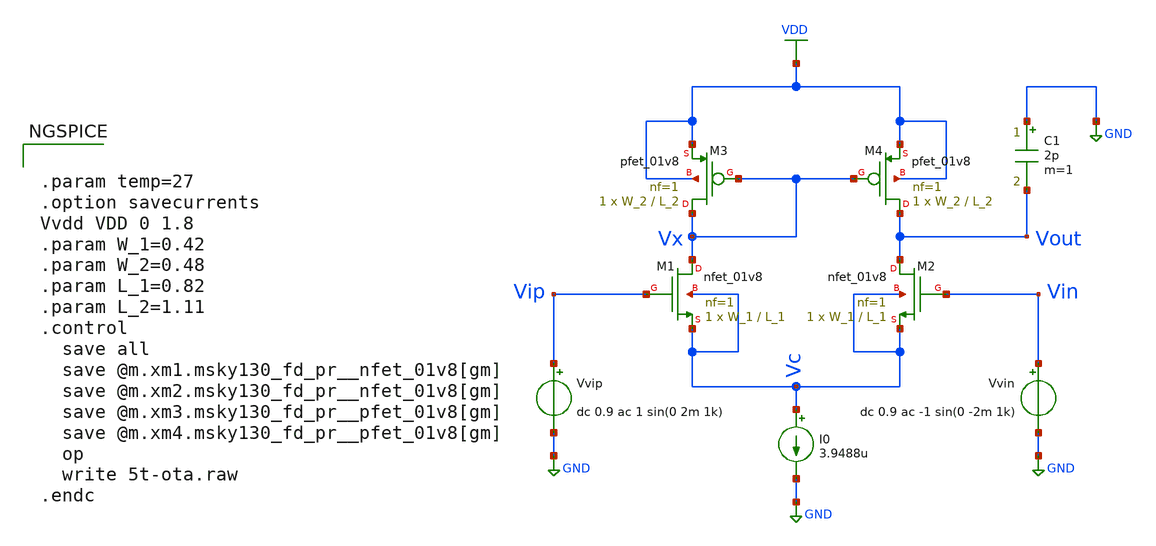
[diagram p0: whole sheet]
** sch_path: Xschem Simulations/5T-OTA/5t-ota.sch
**.subckt 5t-ota
XM1 Vx Vip Vc Vc sky130_fd_pr__nfet_01v8 L=L_1 W=W_1 nf=1 ad='int((1 + 1)/2) * W_1 / 1 * 0.29' as='int((1 + 2)/2) * W_1 / 1 * 0.29'
+ pd='2*int((1 + 1)/2) * (W_1 / 1 + 0.29)' ps='2*int((1 + 2)/2) * (W_1 / 1 + 0.29)' nrd='0.29 / W_1 ' nrs='0.29 / W_1 '
+ sa=0 sb=0 sd=0 mult=1 m=1
XM2 Vout Vin Vc Vc sky130_fd_pr__nfet_01v8 L=L_1 W=W_1 nf=1 ad='int((1 + 1)/2) * W_1 / 1 * 0.29' as='int((1 + 2)/2) * W_1 / 1 * 0.29'
+ pd='2*int((1 + 1)/2) * (W_1 / 1 + 0.29)' ps='2*int((1 + 2)/2) * (W_1 / 1 + 0.29)' nrd='0.29 / W_1 ' nrs='0.29 / W_1 '
+ sa=0 sb=0 sd=0 mult=1 m=1
I0 Vc GND 3.9488u
Vvip Vip GND dc 0.9 ac 1 sin(0 2m 1k)
Vvin Vin GND dc 0.9 ac -1 sin(0 -2m 1k)
C1 GND Vout 2p m=1
XM3 Vx Vx VDD VDD sky130_fd_pr__pfet_01v8 L=L_2 W=W_2 nf=1 ad='int((1 + 1)/2) * W_2 / 1 * 0.29' as='int((1 + 2)/2) * W_2 / 1 * 0.29'
+ pd='2*int((1 + 1)/2) * (W_2 / 1 + 0.29)' ps='2*int((1 + 2)/2) * (W_2 / 1 + 0.29)' nrd='0.29 / W_2 ' nrs='0.29 / W_2 '
+ sa=0 sb=0 sd=0 mult=1 m=1
XM4 Vout Vx VDD VDD sky130_fd_pr__pfet_01v8 L=L_2 W=W_2 nf=1 ad='int((1 + 1)/2) * W_2 / 1 * 0.29' as='int((1 + 2)/2) * W_2 / 1 * 0.29'
+ pd='2*int((1 + 1)/2) * (W_2 / 1 + 0.29)' ps='2*int((1 + 2)/2) * (W_2 / 1 + 0.29)' nrd='0.29 / W_2 ' nrs='0.29 / W_2 '
+ sa=0 sb=0 sd=0 mult=1 m=1
**** begin user architecture code

** opencircuitdesign pdks install
.lib $::SKYWATER_MODELS/sky130.lib.spice tt



.param temp=27
.option savecurrents
Vvdd VDD 0 1.8
.param W_1=0.42
.param W_2=0.48
.param L_1=0.82
.param L_2=1.11
.control
  save all
  save @m.xm1.msky130_fd_pr__nfet_01v8[gm]
  save @m.xm2.msky130_fd_pr__nfet_01v8[gm]
  save @m.xm3.msky130_fd_pr__pfet_01v8[gm]
  save @m.xm4.msky130_fd_pr__pfet_01v8[gm]
  op
  write 5t-ota.raw
.endc




.control
  tran 1u 5m
  save all

  let v_input = v(vip) - v(vin)
  let v_output = v(vout)

  plot v_input
  plot v_output

  meas tran v_in_pk  PP v_input from=1m to=5m
  meas tran v_out_pk PP v_output from=1m to=5m

  let voltage_gain = v_out_pk / v_in_pk
  print voltage_gain
.endc




.control
  alter Vvin pulse = [ 898m 902m 0 10p 10p 0.5m 1m 1 ]
  alter Vvip pulse = [ 902m 898m 0 10p 10p 0.5m 1m 1 ]
  tran 0.1n 600u 450u
  save all

  plot (v(vip) - v(vin))
  plot v(vout)

  meas tran v_max FIND v(vout) AT=590u
  meas tran v_min FIND v(vout) AT=460u

  let v10 = v_min + (0.1*(v_max-v_min))
  let v90 = v_max - (0.1*(v_max-v_min))
  meas tran t10 WHEN v(vout)=v10 RISE=1
  meas tran t90 WHEN v(vout)=v90 RISE=1

  let slew_rate = ((v90 - v10) / (t90 - t10)) * 1e-6
  print slew_rate
.endc




.control
  ac dec 100 0.1 1G
  save all

  let gain = v(vout) / (v(vip) - v(vin))
  let db_gain = db(gain)
  let deg_phase = 180*cph(v(vout))/pi

  meas ac gbw_freq WHEN db_gain=0 FALL=1
  let gbw_Mfreq = gbw_freq * 1e-6

  meas ac pm_deg FIND deg_phase AT=gbw_freq
  let pm = 180 + pm_deg

  plot db_gain deg_phase
  print gbw_Mfreq
  print pm
.endc


**** end user architecture code
**.ends
.GLOBAL GND
.GLOBAL VDD
.end
